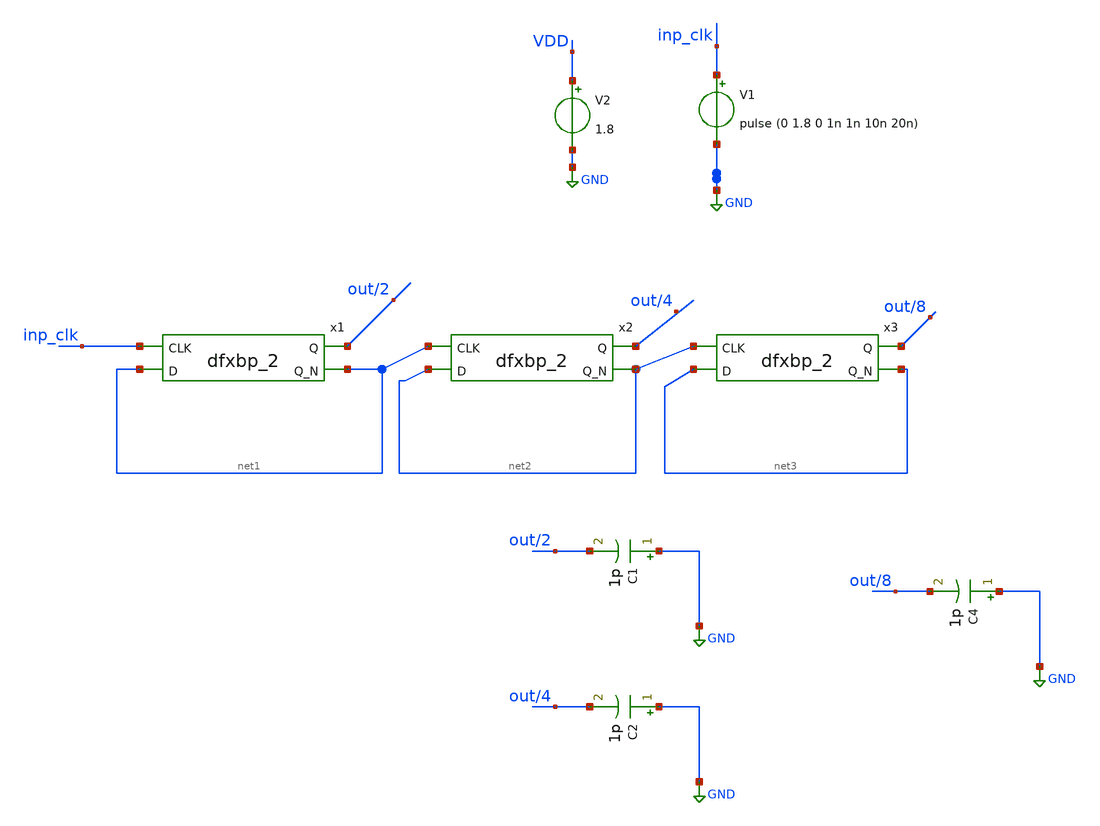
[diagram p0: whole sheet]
** sch_path: xschem/divi_v0.sch
.lib $::SKYWATER_MODELS/sky130.lib.spice tt
.include $::SKYWATER_STDCELLS/sky130_fd_sc_hd.spice

**.subckt divi_v0
x1 inp_clk net1 GND GND VDD VDD out/2 net1 sky130_fd_sc_hd__dfxbp_2
V2 VDD GND 1.8
V1 inp_clk GND pulse (0 1.8 0 1n 1n 10n 20n)
C4 GND out/8 1p m=1
C1 GND out/2 1p m=1
C2 GND out/4 1p m=1
x2 net1 net2 GND GND VDD VDD net4 net2 sky130_fd_sc_hd__dfxbp_2
x3 net2 net3 GND GND VDD VDD out/8 net3 sky130_fd_sc_hd__dfxbp_2
**** begin user architecture code


.control
save all
tran 0.1n 100n
write divi_v0.raw
*quit
plot v(inp_clk) v(out/2)  v(out/8) v(out/4)
.endc


**** end user architecture code
**.ends
.GLOBAL GND
.end
